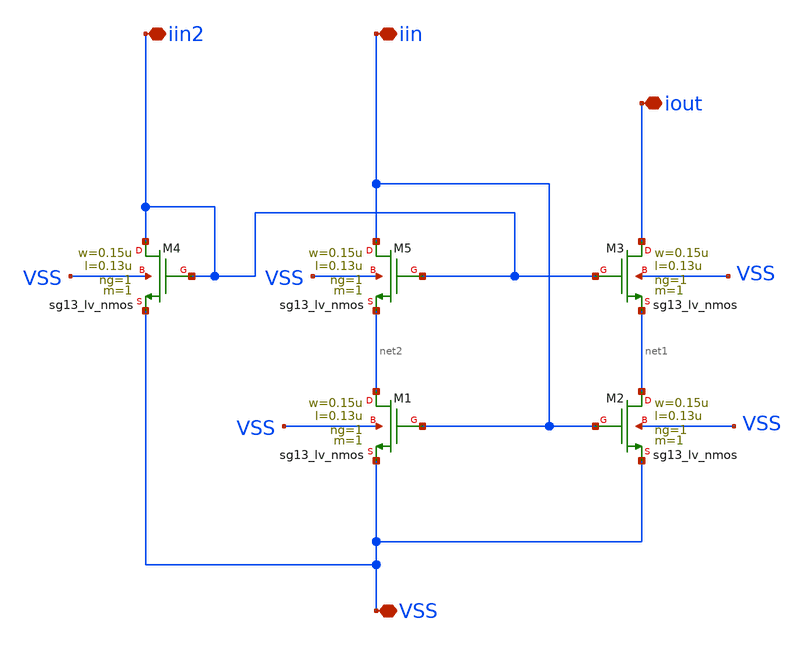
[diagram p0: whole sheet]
** sch_path: analog-db/templates/current_mirror/nmos_current_sink/improved_high_swing_cascode_current_mirror.sch
* Copyright 2026 MacAnalog Research Group
**.subckt improved_high_swing_cascode_current_mirror VSS iin iout iin2
*.iopin VSS
*.iopin iin
*.iopin iout
*.iopin iin2
XM1 net2 iin VSS VSS sg13_lv_nmos w=0.15u l=0.13u ng=1 m=1 mm_ok=1
XM2 net1 iin VSS VSS sg13_lv_nmos w=0.15u l=0.13u ng=1 m=1 mm_ok=1
XM3 iout iin2 net1 VSS sg13_lv_nmos w=0.15u l=0.13u ng=1 m=1 mm_ok=1
XM4 iin2 iin2 VSS VSS sg13_lv_nmos w=0.15u l=0.13u ng=1 m=1 mm_ok=1
XM5 iin iin2 net2 VSS sg13_lv_nmos w=0.15u l=0.13u ng=1 m=1 mm_ok=1
**.ends
.end
